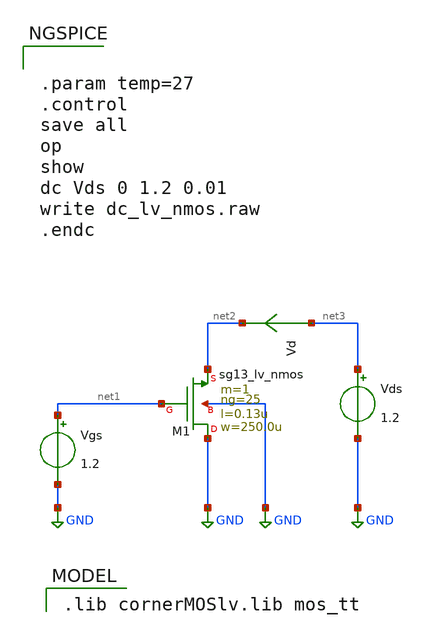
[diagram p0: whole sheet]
** sch_path: CHIPCHILE_CANELOS24_WorkshopTO/design_data/xschem/tgate/dc_lv_nmos.sch
* Copyright 2023 IHP PDK Authors
**.subckt dc_lv_nmos
Vgs net1 GND 1.2
Vds net3 GND 1.2
Vd net3 net2 0
.save i(vd)
XM1 GND net1 net2 GND sg13_lv_nmos w=250.0u l=0.13u ng=25 m=1 mm_ok=1
**** begin user architecture code
 .lib cornerMOSlv.lib mos_tt



.param temp=27
.control
save all
op
show
dc Vds 0 1.2 0.01
write dc_lv_nmos.raw
.endc


**** end user architecture code
**.ends
.GLOBAL GND
.end
